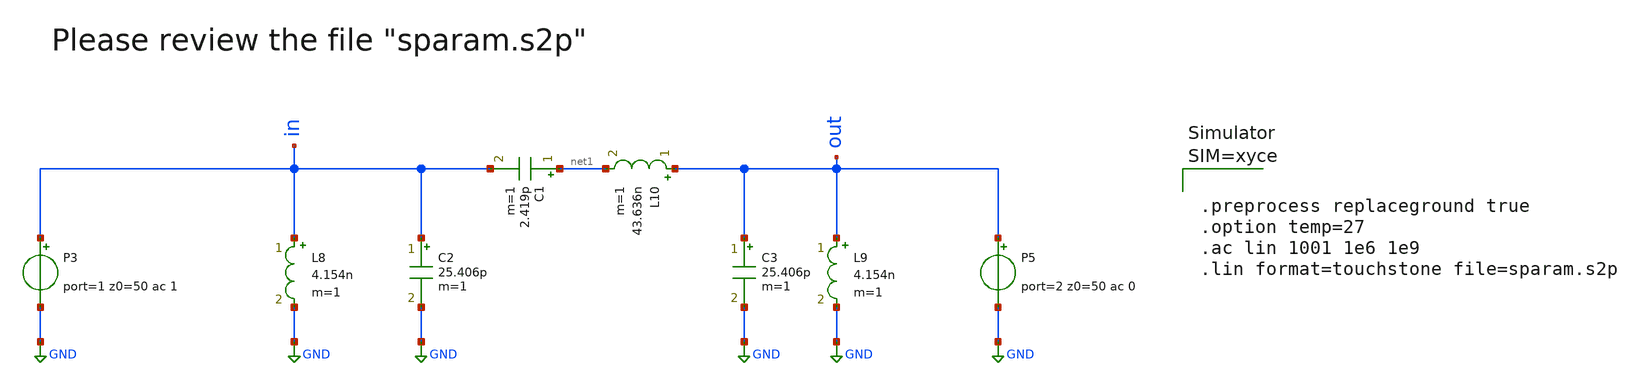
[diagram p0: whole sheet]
** sch_path: ihp-sg13g2/libs.tech/xschem/sg13g2_tests_xyce/sp_singleport.sch
* Copyright 2021 Stefan Frederik Schippers
* Licensed under the Apache License, Version 2.0 (the "License");
* you may not use this file except in compliance with the License.
* You may obtain a copy of the License at
* https://www.apache.org/licenses/LICENSE-2.0
* Unless required by applicable law or agreed to in writing, software
* distributed under the License is distributed on an "AS IS" BASIS,
* WITHOUT WARRANTIES OR CONDITIONS OF ANY KIND, either express or implied.
* See the License for the specific language governing permissions and
* limitations under the License.
* Copyright 2023 IHP PDK Authors
**.subckt sp_singleport
P3 in GND port=1 z0=50 ac 1
P5 out GND port=2 z0=50 ac 0
C1 net1 in 2.419p m=1
C2 in GND 25.406p m=1
C3 out GND 25.406p m=1
L8 in GND 4.154n m=1
L9 out GND 4.154n m=1
L10 out net1 43.636n m=1
**** begin user architecture code



**** end user architecture code
**.ends
.GLOBAL GND
.end
